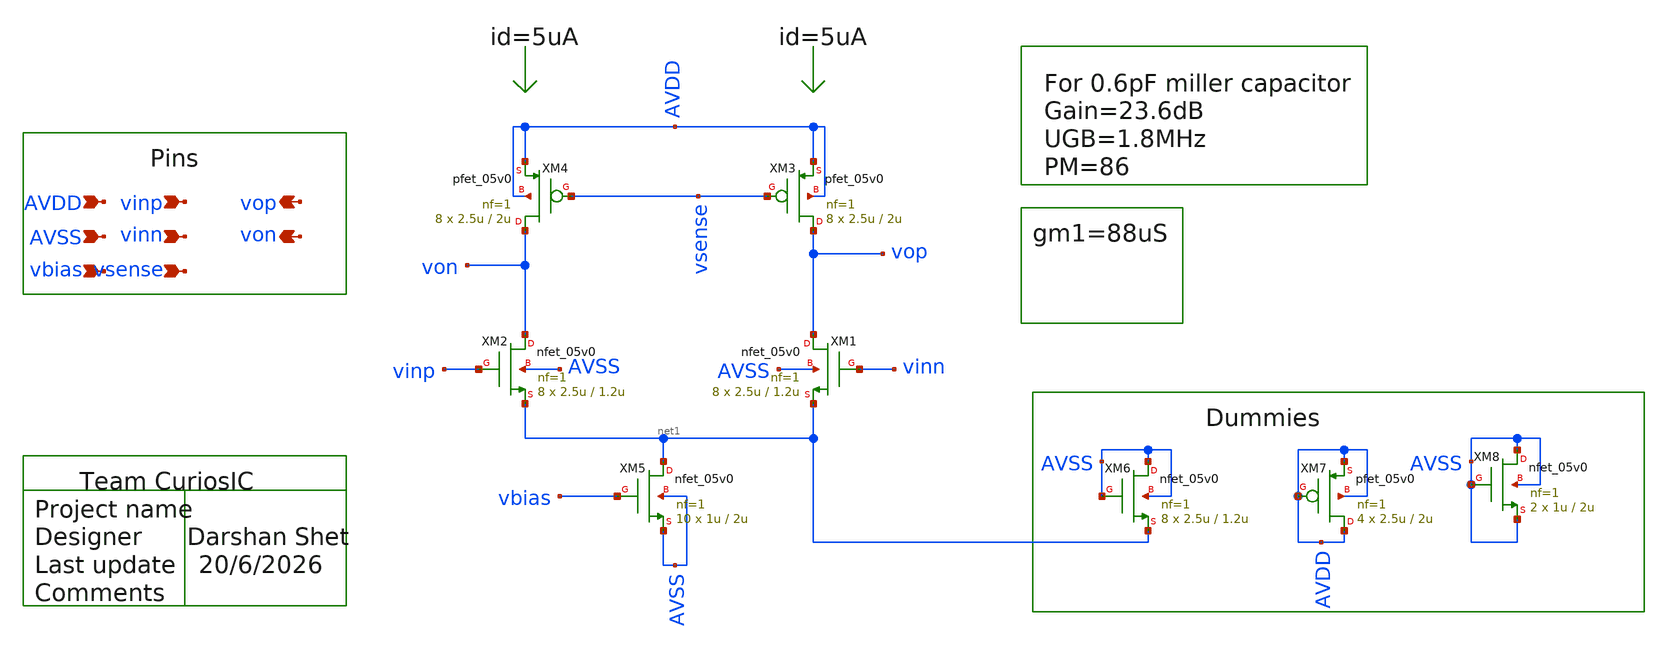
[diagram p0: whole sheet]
** sch_path: design/schematics/CCIA/Instrumentation Amplifier/DS_cic_bms_inst_amp_gm1.sch
**.subckt DS_cic_bms_inst_amp_gm1 vinp vinn von vop AVDD AVSS vsense vbias
*.ipin vinp
*.ipin vinn
*.opin von
*.opin vop
*.ipin AVDD
*.ipin AVSS
*.ipin vsense
*.ipin vbias
XM1 vop vinn net1 AVSS nfet_05v0 L=1.2u W=2.5u nf=1 ad='int((nf+1)/2) * W/nf * 0.18u' as='int((nf+2)/2) * W/nf * 0.18u'
+ pd='2*int((nf+1)/2) * (W/nf + 0.18u)' ps='2*int((nf+2)/2) * (W/nf + 0.18u)' nrd='0.18u / W' nrs='0.18u / W'
+ sa=0 sb=0 sd=0 m=8
XM2 von vinp net1 AVSS nfet_05v0 L=1.2u W=2.5u nf=1 ad='int((nf+1)/2) * W/nf * 0.18u' as='int((nf+2)/2) * W/nf * 0.18u'
+ pd='2*int((nf+1)/2) * (W/nf + 0.18u)' ps='2*int((nf+2)/2) * (W/nf + 0.18u)' nrd='0.18u / W' nrs='0.18u / W'
+ sa=0 sb=0 sd=0 m=8
XM3 vop vsense AVDD AVDD pfet_05v0 L=2u W=2.5u nf=1 ad='int((nf+1)/2) * W/nf * 0.18u' as='int((nf+2)/2) * W/nf * 0.18u'
+ pd='2*int((nf+1)/2) * (W/nf + 0.18u)' ps='2*int((nf+2)/2) * (W/nf + 0.18u)' nrd='0.18u / W' nrs='0.18u / W'
+ sa=0 sb=0 sd=0 m=8
XM4 von vsense AVDD AVDD pfet_05v0 L=2u W=2.5u nf=1 ad='int((nf+1)/2) * W/nf * 0.18u' as='int((nf+2)/2) * W/nf * 0.18u'
+ pd='2*int((nf+1)/2) * (W/nf + 0.18u)' ps='2*int((nf+2)/2) * (W/nf + 0.18u)' nrd='0.18u / W' nrs='0.18u / W'
+ sa=0 sb=0 sd=0 m=8
XM5 net1 vbias AVSS AVSS nfet_05v0 L=2u W=1u nf=1 ad='int((nf+1)/2) * W/nf * 0.18u' as='int((nf+2)/2) * W/nf * 0.18u'
+ pd='2*int((nf+1)/2) * (W/nf + 0.18u)' ps='2*int((nf+2)/2) * (W/nf + 0.18u)' nrd='0.18u / W' nrs='0.18u / W'
+ sa=0 sb=0 sd=0 m=10
XM6 AVSS AVSS net1 AVSS nfet_05v0 L=1.2u W=2.5u nf=1 ad='int((nf+1)/2) * W/nf * 0.18u' as='int((nf+2)/2) * W/nf * 0.18u'
+ pd='2*int((nf+1)/2) * (W/nf + 0.18u)' ps='2*int((nf+2)/2) * (W/nf + 0.18u)' nrd='0.18u / W' nrs='0.18u / W'
+ sa=0 sb=0 sd=0 m=8
XM7 AVDD AVDD AVDD AVDD pfet_05v0 L=2u W=2.5u nf=1 ad='int((nf+1)/2) * W/nf * 0.18u' as='int((nf+2)/2) * W/nf * 0.18u'
+ pd='2*int((nf+1)/2) * (W/nf + 0.18u)' ps='2*int((nf+2)/2) * (W/nf + 0.18u)' nrd='0.18u / W' nrs='0.18u / W'
+ sa=0 sb=0 sd=0 m=4
XM8 AVSS AVSS AVSS AVSS nfet_05v0 L=2u W=1u nf=1 ad='int((nf+1)/2) * W/nf * 0.18u' as='int((nf+2)/2) * W/nf * 0.18u'
+ pd='2*int((nf+1)/2) * (W/nf + 0.18u)' ps='2*int((nf+2)/2) * (W/nf + 0.18u)' nrd='0.18u / W' nrs='0.18u / W'
+ sa=0 sb=0 sd=0 m=2
**.ends
.end
